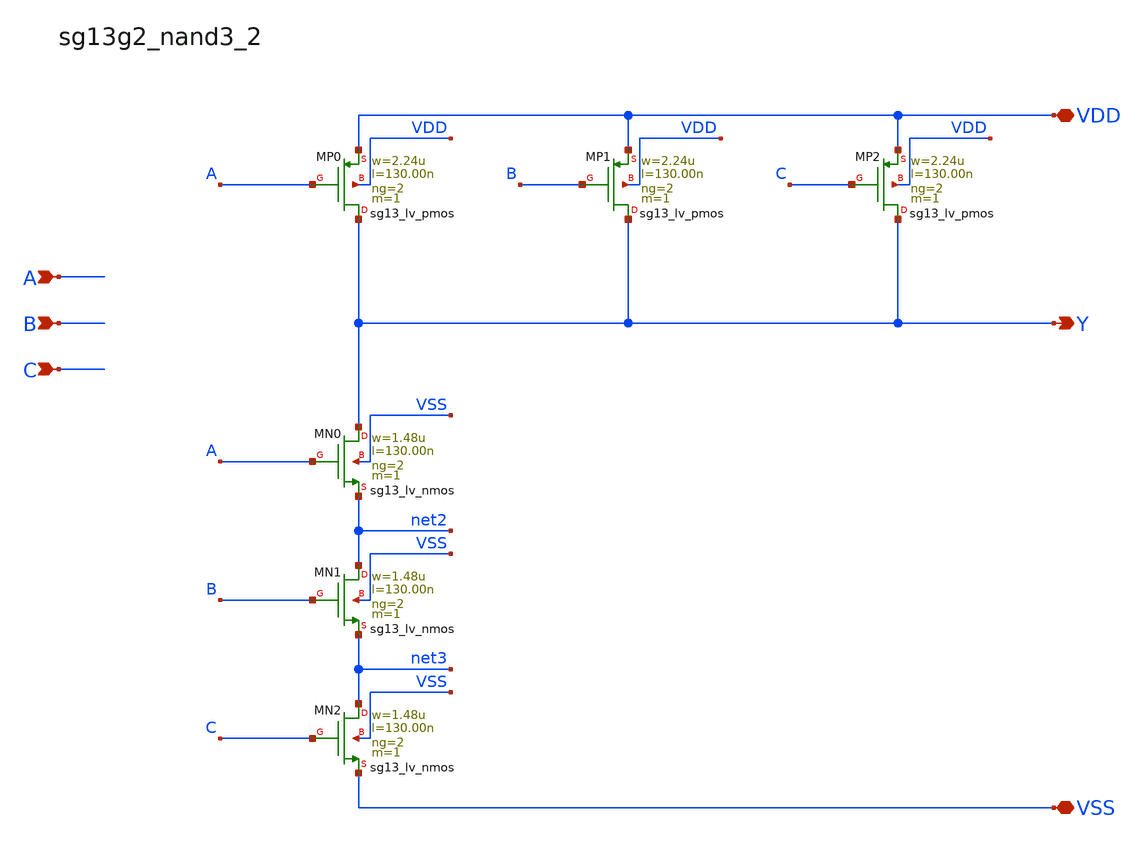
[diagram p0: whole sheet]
** sch_path: outputs/sg13g2_cells/cells/sg13g2_nand3_2/sg13g2_nand3_2.sch
**.subckt sg13g2_nand3_2 Y A B C VDD VSS
*.opin Y
*.ipin A
*.ipin B
*.ipin C
*.iopin VDD
*.iopin VSS
XMP0 Y A VDD VDD sg13_lv_pmos w=2.24u l=130.00n ng=2 m=1 mm_ok=1
XMP1 Y B VDD VDD sg13_lv_pmos w=2.24u l=130.00n ng=2 m=1 mm_ok=1
XMP2 Y C VDD VDD sg13_lv_pmos w=2.24u l=130.00n ng=2 m=1 mm_ok=1
XMN1 net2 B net3 VSS sg13_lv_nmos w=1.48u l=130.00n ng=2 m=1 mm_ok=1
XMN2 net3 C VSS VSS sg13_lv_nmos w=1.48u l=130.00n ng=2 m=1 mm_ok=1
XMN0 Y A net2 VSS sg13_lv_nmos w=1.48u l=130.00n ng=2 m=1 mm_ok=1
**.ends
.end
